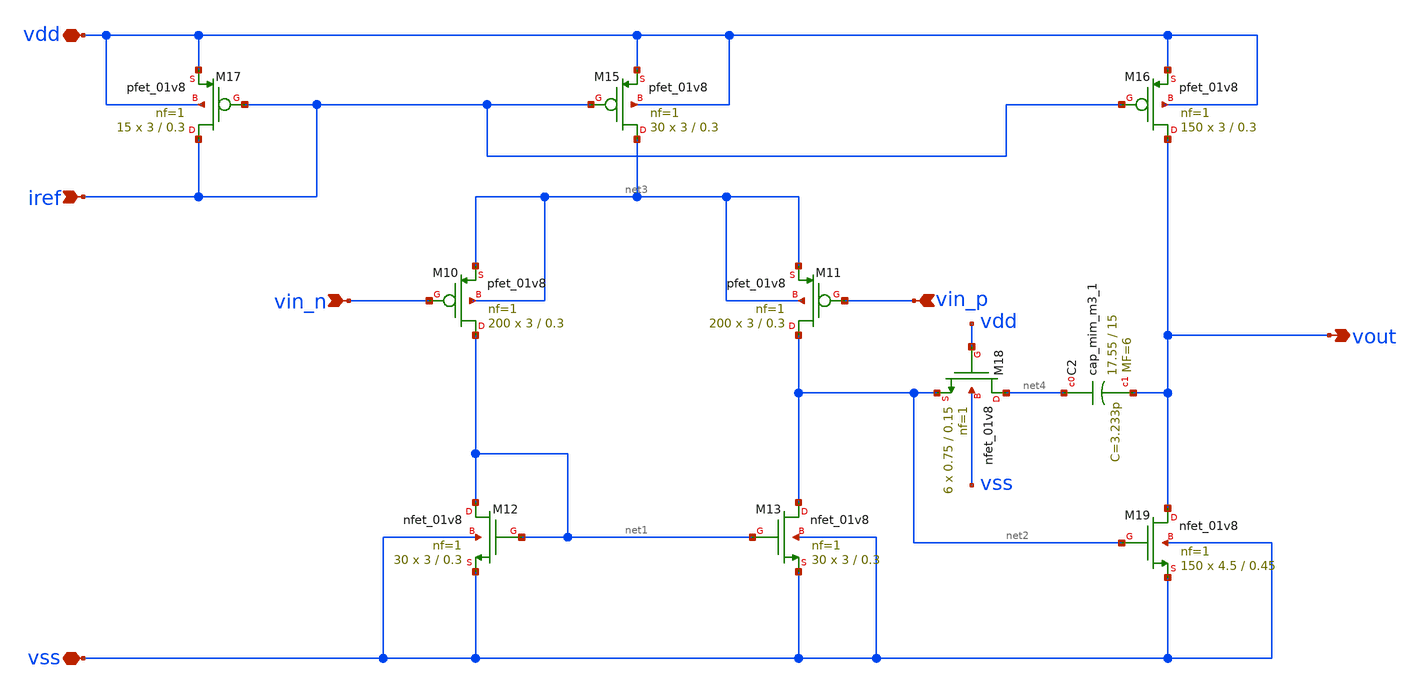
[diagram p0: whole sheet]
** sch_path: xschem/Vth_sch/op-amp_2.sch
**.subckt op-amp_2 vdd vss vin_n vin_p iref vout
*.iopin vdd
*.iopin vss
*.ipin vin_n
*.ipin vin_p
*.ipin iref
*.opin vout
XM10 net1 vin_n net3 net3 sky130_fd_pr__pfet_01v8 L=0.3 W=3 nf=1 ad='W * 0.29' as='W * 0.29' pd='2 * (W + 0.29)'
+ ps='2 * (W + 0.29)' nrd='0.29 / W' nrs='0.29 / W' sa=0 sb=0 sd=0 mult=200 m=200
XM11 net2 vin_p net3 net3 sky130_fd_pr__pfet_01v8 L=0.3 W=3 nf=1 ad='W * 0.29' as='W * 0.29' pd='2 * (W + 0.29)'
+ ps='2 * (W + 0.29)' nrd='0.29 / W' nrs='0.29 / W' sa=0 sb=0 sd=0 mult=200 m=200
XM12 net1 net1 vss vss sky130_fd_pr__nfet_01v8 L=0.3 W=3 nf=1 ad='W * 0.29' as='W * 0.29' pd='2 * (W + 0.29)'
+ ps='2 * (W + 0.29)' nrd='0.29 / W' nrs='0.29 / W' sa=0 sb=0 sd=0 mult=30 m=30
XM13 net2 net1 vss vss sky130_fd_pr__nfet_01v8 L=0.3 W=3 nf=1 ad='W * 0.29' as='W * 0.29' pd='2 * (W + 0.29)'
+ ps='2 * (W + 0.29)' nrd='0.29 / W' nrs='0.29 / W' sa=0 sb=0 sd=0 mult=30 m=30
XM15 net3 iref vdd vdd sky130_fd_pr__pfet_01v8 L=0.3 W=3 nf=1 ad='W * 0.29' as='W * 0.29' pd='2 * (W + 0.29)'
+ ps='2 * (W + 0.29)' nrd='0.29 / W' nrs='0.29 / W' sa=0 sb=0 sd=0 mult=30 m=30
XM16 vout iref vdd vdd sky130_fd_pr__pfet_01v8 L=0.3 W=3 nf=1 ad='W * 0.29' as='W * 0.29' pd='2 * (W + 0.29)'
+ ps='2 * (W + 0.29)' nrd='0.29 / W' nrs='0.29 / W' sa=0 sb=0 sd=0 mult=150 m=150
XM17 iref iref vdd vdd sky130_fd_pr__pfet_01v8 L=0.3 W=3 nf=1 ad='W * 0.29' as='W * 0.29' pd='2 * (W + 0.29)'
+ ps='2 * (W + 0.29)' nrd='0.29 / W' nrs='0.29 / W' sa=0 sb=0 sd=0 mult=15 m=15
XM18 net4 vdd net2 vss sky130_fd_pr__nfet_01v8 L=0.15 W=0.75 nf=1 ad='W * 0.29' as='W * 0.29' pd='2 * (W + 0.29)'
+ ps='2 * (W + 0.29)' nrd='0.29 / W' nrs='0.29 / W' sa=0 sb=0 sd=0 mult=6 m=6
XC2 net4 vout sky130_fd_pr__cap_mim_m3_1 W=17.55 L=15 MF=6 m=6
XM19 vout net2 vss vss sky130_fd_pr__nfet_01v8 L=0.45 W=4.5 nf=1 ad='W * 0.29' as='W * 0.29' pd='2 * (W + 0.29)'
+ ps='2 * (W + 0.29)' nrd='0.29 / W' nrs='0.29 / W' sa=0 sb=0 sd=0 mult=150 m=150
**.ends
.end
